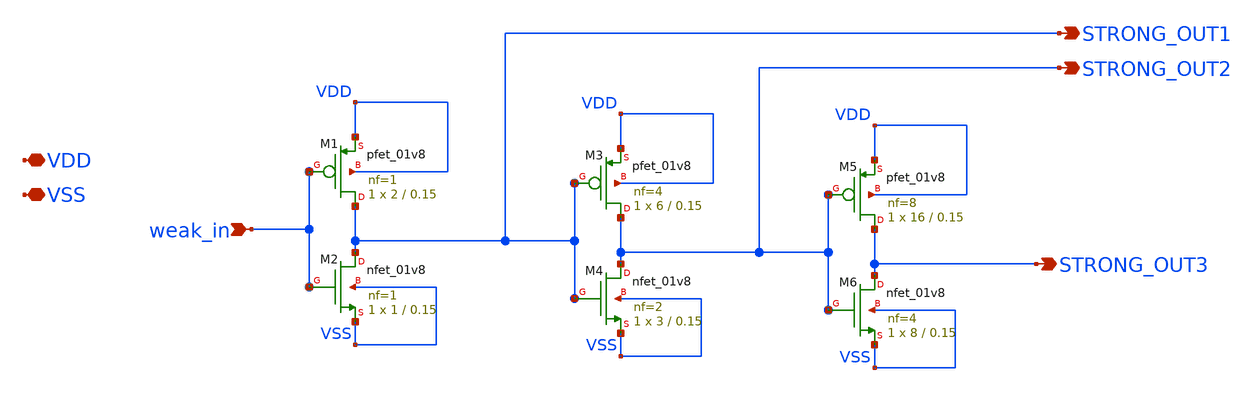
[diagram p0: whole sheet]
** sch_path: xschem/inverter_chain.sch
**.subckt inverter_chain VDD VSS weak_in STRONG_OUT3 STRONG_OUT2 STRONG_OUT1
*.iopin VDD
*.iopin VSS
*.ipin weak_in
*.opin STRONG_OUT3
*.opin STRONG_OUT2
*.opin STRONG_OUT1
XM1 STRONG_OUT1 weak_in VDD VDD sky130_fd_pr__pfet_01v8 L=0.15 W=2 nf=1 ad='int((nf+1)/2) * W/nf * 0.29'
+ as='int((nf+2)/2) * W/nf * 0.29' pd='2*int((nf+1)/2) * (W/nf + 0.29)' ps='2*int((nf+2)/2) * (W/nf + 0.29)'
+ nrd='0.29 / W' nrs='0.29 / W' sa=0 sb=0 sd=0 mult=1 m=1
XM2 STRONG_OUT1 weak_in VSS VSS sky130_fd_pr__nfet_01v8 L=0.15 W=1 nf=1 ad='int((nf+1)/2) * W/nf * 0.29'
+ as='int((nf+2)/2) * W/nf * 0.29' pd='2*int((nf+1)/2) * (W/nf + 0.29)' ps='2*int((nf+2)/2) * (W/nf + 0.29)'
+ nrd='0.29 / W' nrs='0.29 / W' sa=0 sb=0 sd=0 mult=1 m=1
XM3 STRONG_OUT2 STRONG_OUT1 VDD VDD sky130_fd_pr__pfet_01v8 L=0.15 W=6 nf=4 ad='int((nf+1)/2) * W/nf * 0.29'
+ as='int((nf+2)/2) * W/nf * 0.29' pd='2*int((nf+1)/2) * (W/nf + 0.29)' ps='2*int((nf+2)/2) * (W/nf + 0.29)'
+ nrd='0.29 / W' nrs='0.29 / W' sa=0 sb=0 sd=0 mult=1 m=1
XM4 STRONG_OUT2 STRONG_OUT1 VSS VSS sky130_fd_pr__nfet_01v8 L=0.15 W=3 nf=2 ad='int((nf+1)/2) * W/nf * 0.29'
+ as='int((nf+2)/2) * W/nf * 0.29' pd='2*int((nf+1)/2) * (W/nf + 0.29)' ps='2*int((nf+2)/2) * (W/nf + 0.29)'
+ nrd='0.29 / W' nrs='0.29 / W' sa=0 sb=0 sd=0 mult=1 m=1
XM5 STRONG_OUT3 STRONG_OUT2 VDD VDD sky130_fd_pr__pfet_01v8 L=0.15 W=16 nf=8 ad='int((nf+1)/2) * W/nf * 0.29'
+ as='int((nf+2)/2) * W/nf * 0.29' pd='2*int((nf+1)/2) * (W/nf + 0.29)' ps='2*int((nf+2)/2) * (W/nf + 0.29)'
+ nrd='0.29 / W' nrs='0.29 / W' sa=0 sb=0 sd=0 mult=1 m=1
XM6 STRONG_OUT3 STRONG_OUT2 VSS VSS sky130_fd_pr__nfet_01v8 L=0.15 W=8 nf=4 ad='int((nf+1)/2) * W/nf * 0.29'
+ as='int((nf+2)/2) * W/nf * 0.29' pd='2*int((nf+1)/2) * (W/nf + 0.29)' ps='2*int((nf+2)/2) * (W/nf + 0.29)'
+ nrd='0.29 / W' nrs='0.29 / W' sa=0 sb=0 sd=0 mult=1 m=1
**.ends
.end
